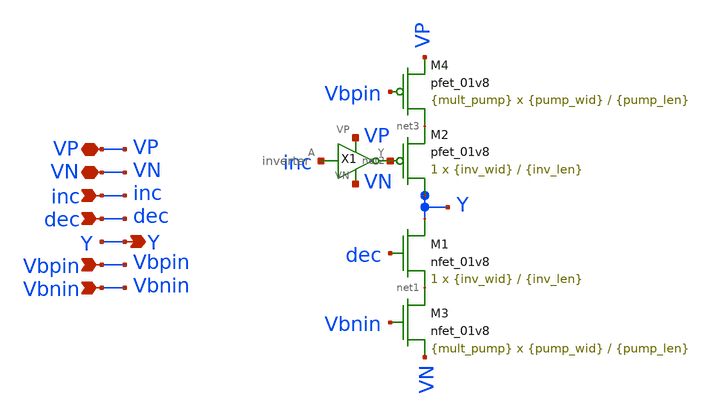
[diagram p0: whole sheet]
** sch_path: ipump.sch
**.subckt ipump VN VP Y Vbpin inc Vbnin dec
*.iopin VN
*.iopin VP
*.opin Y
*.ipin Vbpin
*.ipin inc
*.ipin Vbnin
*.ipin dec
XM1 Y dec net1 VN sky130_fd_pr__nfet_01v8 L={inv_len} W={inv_wid} nf=1 ad='int((nf+1)/2) * W/nf * 0.29'
+ as='int((nf+2)/2) * W/nf * 0.29' pd='2*int((nf+1)/2) * (W/nf + 0.29)' ps='2*int((nf+2)/2) * (W/nf + 0.29)'
+ nrd='0.29 / W' nrs='0.29 / W' sa=0 sb=0 sd=0 mult=1 m=1
XM2 Y net2 net3 VP sky130_fd_pr__pfet_01v8 L={inv_len} W={inv_wid} nf=1 ad='int((nf+1)/2) * W/nf * 0.29'
+ as='int((nf+2)/2) * W/nf * 0.29' pd='2*int((nf+1)/2) * (W/nf + 0.29)' ps='2*int((nf+2)/2) * (W/nf + 0.29)'
+ nrd='0.29 / W' nrs='0.29 / W' sa=0 sb=0 sd=0 mult=1 m=1
XM3 net1 Vbnin VN VN sky130_fd_pr__nfet_01v8 L={pump_len} W={pump_wid} nf=1 ad='int((nf+1)/2) * W/nf * 0.29'
+ as='int((nf+2)/2) * W/nf * 0.29' pd='2*int((nf+1)/2) * (W/nf + 0.29)' ps='2*int((nf+2)/2) * (W/nf + 0.29)'
+ nrd='0.29 / W' nrs='0.29 / W' sa=0 sb=0 sd=0 mult={mult_pump} m={mult_pump}
XM4 net3 Vbpin VP VP sky130_fd_pr__pfet_01v8 L={pump_len} W={pump_wid} nf=1 ad='int((nf+1)/2) * W/nf * 0.29'
+ as='int((nf+2)/2) * W/nf * 0.29' pd='2*int((nf+1)/2) * (W/nf + 0.29)' ps='2*int((nf+2)/2) * (W/nf + 0.29)'
+ nrd='0.29 / W' nrs='0.29 / W' sa=0 sb=0 sd=0 mult={mult_pump} m={mult_pump}
X1 inc net2 VP VN inverter
**.ends

* expanding   symbol:  inverter.sym # of pins=4
** sym_path: inverter.sym
** sch_path: inverter.sch
.subckt inverter A Y VP VN
*.iopin VP
*.ipin A
*.opin Y
*.iopin VN
XM2 Y A VP VP sky130_fd_pr__pfet_01v8 L={inv_len} W={inv_wid} nf=1 ad='int((nf+1)/2) * W/nf * 0.29' as='int((nf+2)/2) * W/nf * 0.29'
+ pd='2*int((nf+1)/2) * (W/nf + 0.29)' ps='2*int((nf+2)/2) * (W/nf + 0.29)' nrd='0.29 / W' nrs='0.29 / W'
+ sa=0 sb=0 sd=0 mult=1 m=1
XM1 Y A VN VN sky130_fd_pr__nfet_01v8 L={inv_len} W={inv_wid} nf=1 ad='int((nf+1)/2) * W/nf * 0.29' as='int((nf+2)/2) * W/nf * 0.29'
+ pd='2*int((nf+1)/2) * (W/nf + 0.29)' ps='2*int((nf+2)/2) * (W/nf + 0.29)' nrd='0.29 / W' nrs='0.29 / W'
+ sa=0 sb=0 sd=0 mult=1 m=1
.ends

.end
